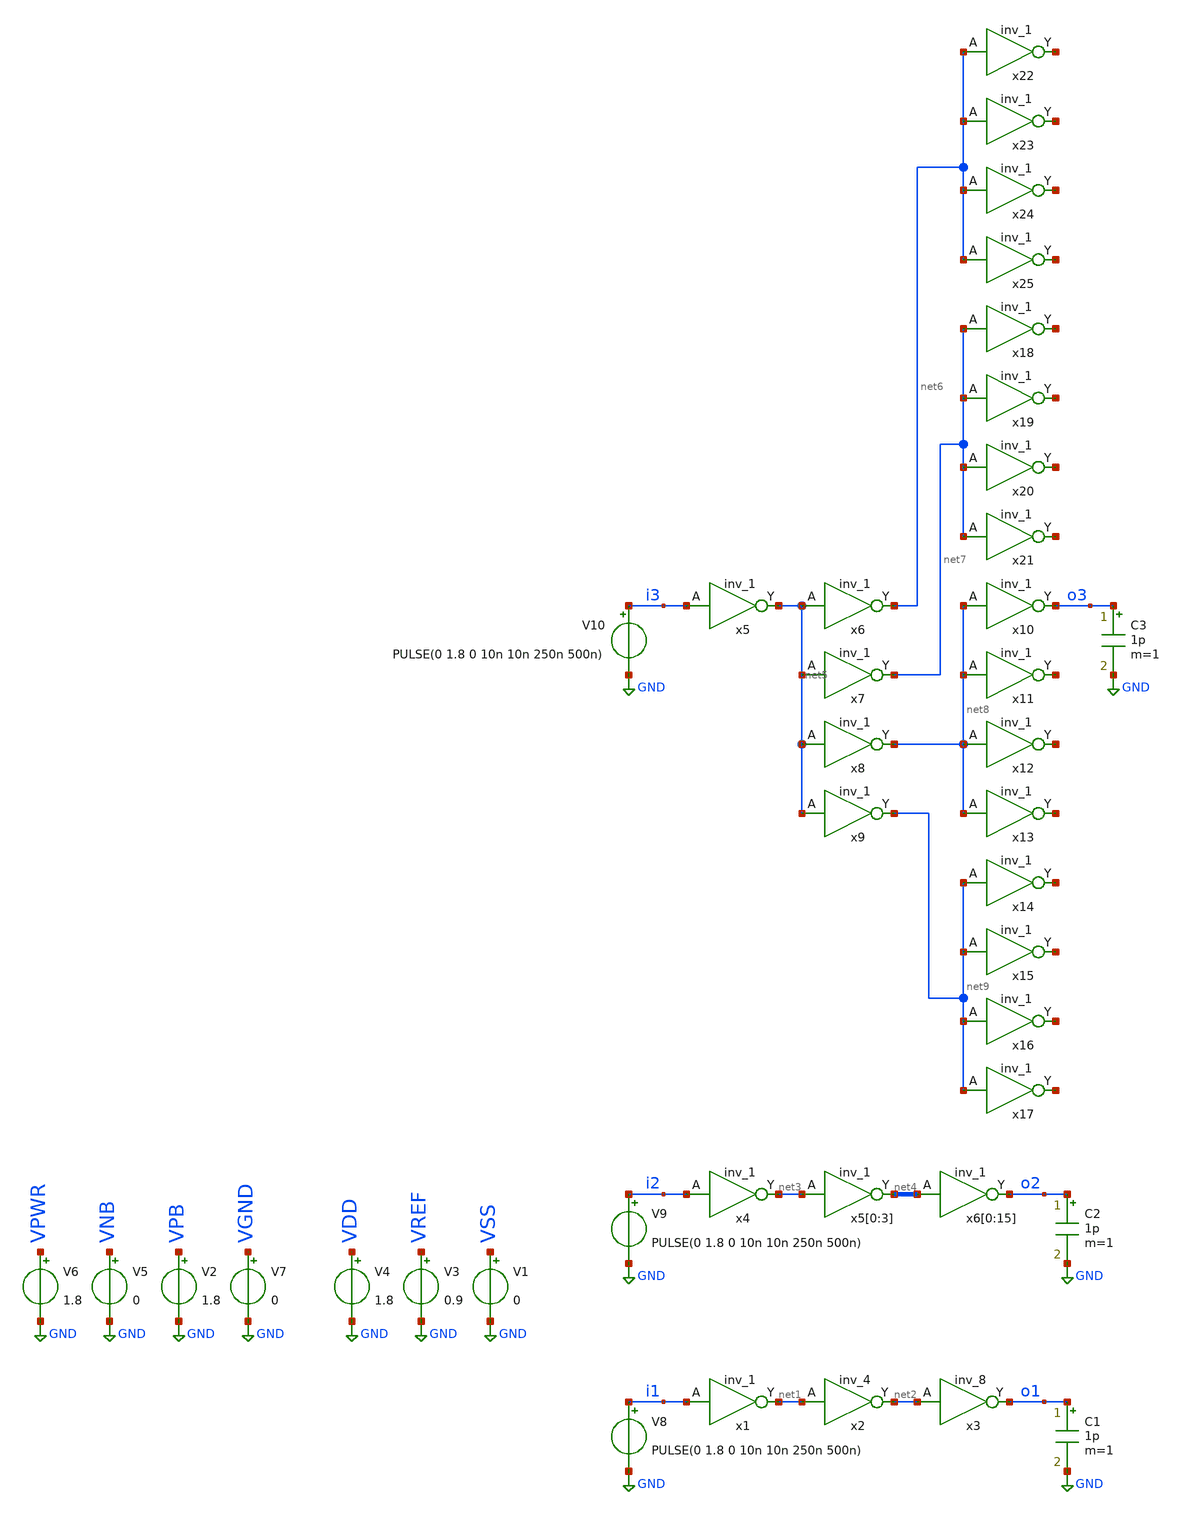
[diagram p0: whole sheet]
** sch_path: tb/untitled.sch
**.subckt untitled
x1 i1 VGND VNB VPB VPWR net1 sky130_fd_sc_hd__inv_1
x2 net1 VGND VNB VPB VPWR net2 sky130_fd_sc_hd__inv_4
x3 net2 VGND VNB VPB VPWR o1 sky130_fd_sc_hd__inv_8
C1 o1 GND 1p m=1
V1 VSS GND 0
V3 VREF GND 0.9
V4 VDD GND 1.8
V2 VPB GND 1.8
V5 VNB GND 0
V6 VPWR GND 1.8
V7 VGND GND 0
V8 i1 GND PULSE(0 1.8 0 10n 10n 250n 500n)
x4 i2 VGND VNB VPB VPWR net3 sky130_fd_sc_hd__inv_1
C2 o2 GND 1p m=1
V9 i2 GND PULSE(0 1.8 0 10n 10n 250n 500n)
x5[0] net3 VGND VNB VPB VPWR net4[3] sky130_fd_sc_hd__inv_1
x5[1] net3 VGND VNB VPB VPWR net4[2] sky130_fd_sc_hd__inv_1
x5[2] net3 VGND VNB VPB VPWR net4[1] sky130_fd_sc_hd__inv_1
x5[3] net3 VGND VNB VPB VPWR net4[0] sky130_fd_sc_hd__inv_1
x6[0] net4[3] VGND VNB VPB VPWR o2 sky130_fd_sc_hd__inv_1
x6[1] net4[2] VGND VNB VPB VPWR o2 sky130_fd_sc_hd__inv_1
x6[2] net4[1] VGND VNB VPB VPWR o2 sky130_fd_sc_hd__inv_1
x6[3] net4[0] VGND VNB VPB VPWR o2 sky130_fd_sc_hd__inv_1
x6[4] net4[3] VGND VNB VPB VPWR o2 sky130_fd_sc_hd__inv_1
x6[5] net4[2] VGND VNB VPB VPWR o2 sky130_fd_sc_hd__inv_1
x6[6] net4[1] VGND VNB VPB VPWR o2 sky130_fd_sc_hd__inv_1
x6[7] net4[0] VGND VNB VPB VPWR o2 sky130_fd_sc_hd__inv_1
x6[8] net4[3] VGND VNB VPB VPWR o2 sky130_fd_sc_hd__inv_1
x6[9] net4[2] VGND VNB VPB VPWR o2 sky130_fd_sc_hd__inv_1
x6[10] net4[1] VGND VNB VPB VPWR o2 sky130_fd_sc_hd__inv_1
x6[11] net4[0] VGND VNB VPB VPWR o2 sky130_fd_sc_hd__inv_1
x6[12] net4[3] VGND VNB VPB VPWR o2 sky130_fd_sc_hd__inv_1
x6[13] net4[2] VGND VNB VPB VPWR o2 sky130_fd_sc_hd__inv_1
x6[14] net4[1] VGND VNB VPB VPWR o2 sky130_fd_sc_hd__inv_1
x6[15] net4[0] VGND VNB VPB VPWR o2 sky130_fd_sc_hd__inv_1
x5 i3 VGND VNB VPB VPWR net5 sky130_fd_sc_hd__inv_1
C3 o3 GND 1p m=1
V10 i3 GND PULSE(0 1.8 0 10n 10n 250n 500n)
x6 net5 VGND VNB VPB VPWR net6 sky130_fd_sc_hd__inv_1
x7 net5 VGND VNB VPB VPWR net7 sky130_fd_sc_hd__inv_1
x8 net5 VGND VNB VPB VPWR net8 sky130_fd_sc_hd__inv_1
x9 net5 VGND VNB VPB VPWR net9 sky130_fd_sc_hd__inv_1
x10 net8 VGND VNB VPB VPWR o3 sky130_fd_sc_hd__inv_1
x11 net8 VGND VNB VPB VPWR net10 sky130_fd_sc_hd__inv_1
x12 net8 VGND VNB VPB VPWR net11 sky130_fd_sc_hd__inv_1
x13 net8 VGND VNB VPB VPWR net12 sky130_fd_sc_hd__inv_1
x14 net9 VGND VNB VPB VPWR net13 sky130_fd_sc_hd__inv_1
x15 net9 VGND VNB VPB VPWR net14 sky130_fd_sc_hd__inv_1
x16 net9 VGND VNB VPB VPWR net15 sky130_fd_sc_hd__inv_1
x17 net9 VGND VNB VPB VPWR net16 sky130_fd_sc_hd__inv_1
x18 net7 VGND VNB VPB VPWR net17 sky130_fd_sc_hd__inv_1
x19 net7 VGND VNB VPB VPWR net18 sky130_fd_sc_hd__inv_1
x20 net7 VGND VNB VPB VPWR net19 sky130_fd_sc_hd__inv_1
x21 net7 VGND VNB VPB VPWR net20 sky130_fd_sc_hd__inv_1
x22 net6 VGND VNB VPB VPWR net21 sky130_fd_sc_hd__inv_1
x23 net6 VGND VNB VPB VPWR net22 sky130_fd_sc_hd__inv_1
x24 net6 VGND VNB VPB VPWR net23 sky130_fd_sc_hd__inv_1
x25 net6 VGND VNB VPB VPWR net24 sky130_fd_sc_hd__inv_1
**** begin user architecture code



.OPTIONS savecurrents
.tran 10ps 350ns
.include /foss/designs/hgu_goss/hgu/mag/hgu_cdac_unit.spice
.lib /foss/pdks/sky130A/libs.tech/ngspice/sky130.lib.spice tt
.include /foss/pdks/sky130A/libs.ref/sky130_fd_sc_hd/spice/sky130_fd_sc_hd.spice

.control
	run
	plot V(i1) V(o1)
	plot V(i2) V(o2)
	plot V(i3) V(o3)

.endc
.save all



**** end user architecture code
**.ends
.GLOBAL GND
.end
